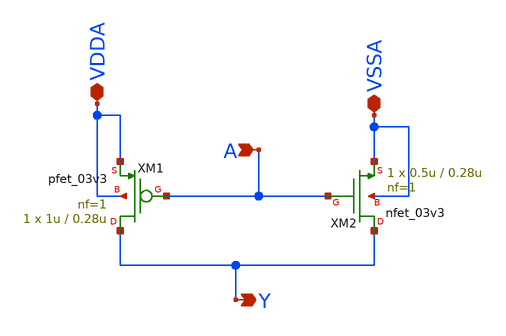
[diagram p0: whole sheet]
** sch_path: xschem/charge_pump/cp_inv.sch
**.subckt cp_inv VDDA VSSA A Y
*.iopin VDDA
*.iopin VSSA
*.ipin A
*.opin Y
XM1 Y A VDDA VDDA pfet_03v3 L=0.28u W=1u nf=1 ad='int((nf+1)/2) * W/nf * 0.18u' as='int((nf+2)/2) * W/nf * 0.18u'
+ pd='2*int((nf+1)/2) * (W/nf + 0.18u)' ps='2*int((nf+2)/2) * (W/nf + 0.18u)' nrd='0.18u / W' nrs='0.18u / W'
+ sa=0 sb=0 sd=0 m=1
XM2 Y A VSSA VSSA nfet_03v3 L=0.28u W=0.5u nf=1 ad='int((nf+1)/2) * W/nf * 0.18u' as='int((nf+2)/2) * W/nf * 0.18u'
+ pd='2*int((nf+1)/2) * (W/nf + 0.18u)' ps='2*int((nf+2)/2) * (W/nf + 0.18u)' nrd='0.18u / W' nrs='0.18u / W'
+ sa=0 sb=0 sd=0 m=1
**.ends
.end
